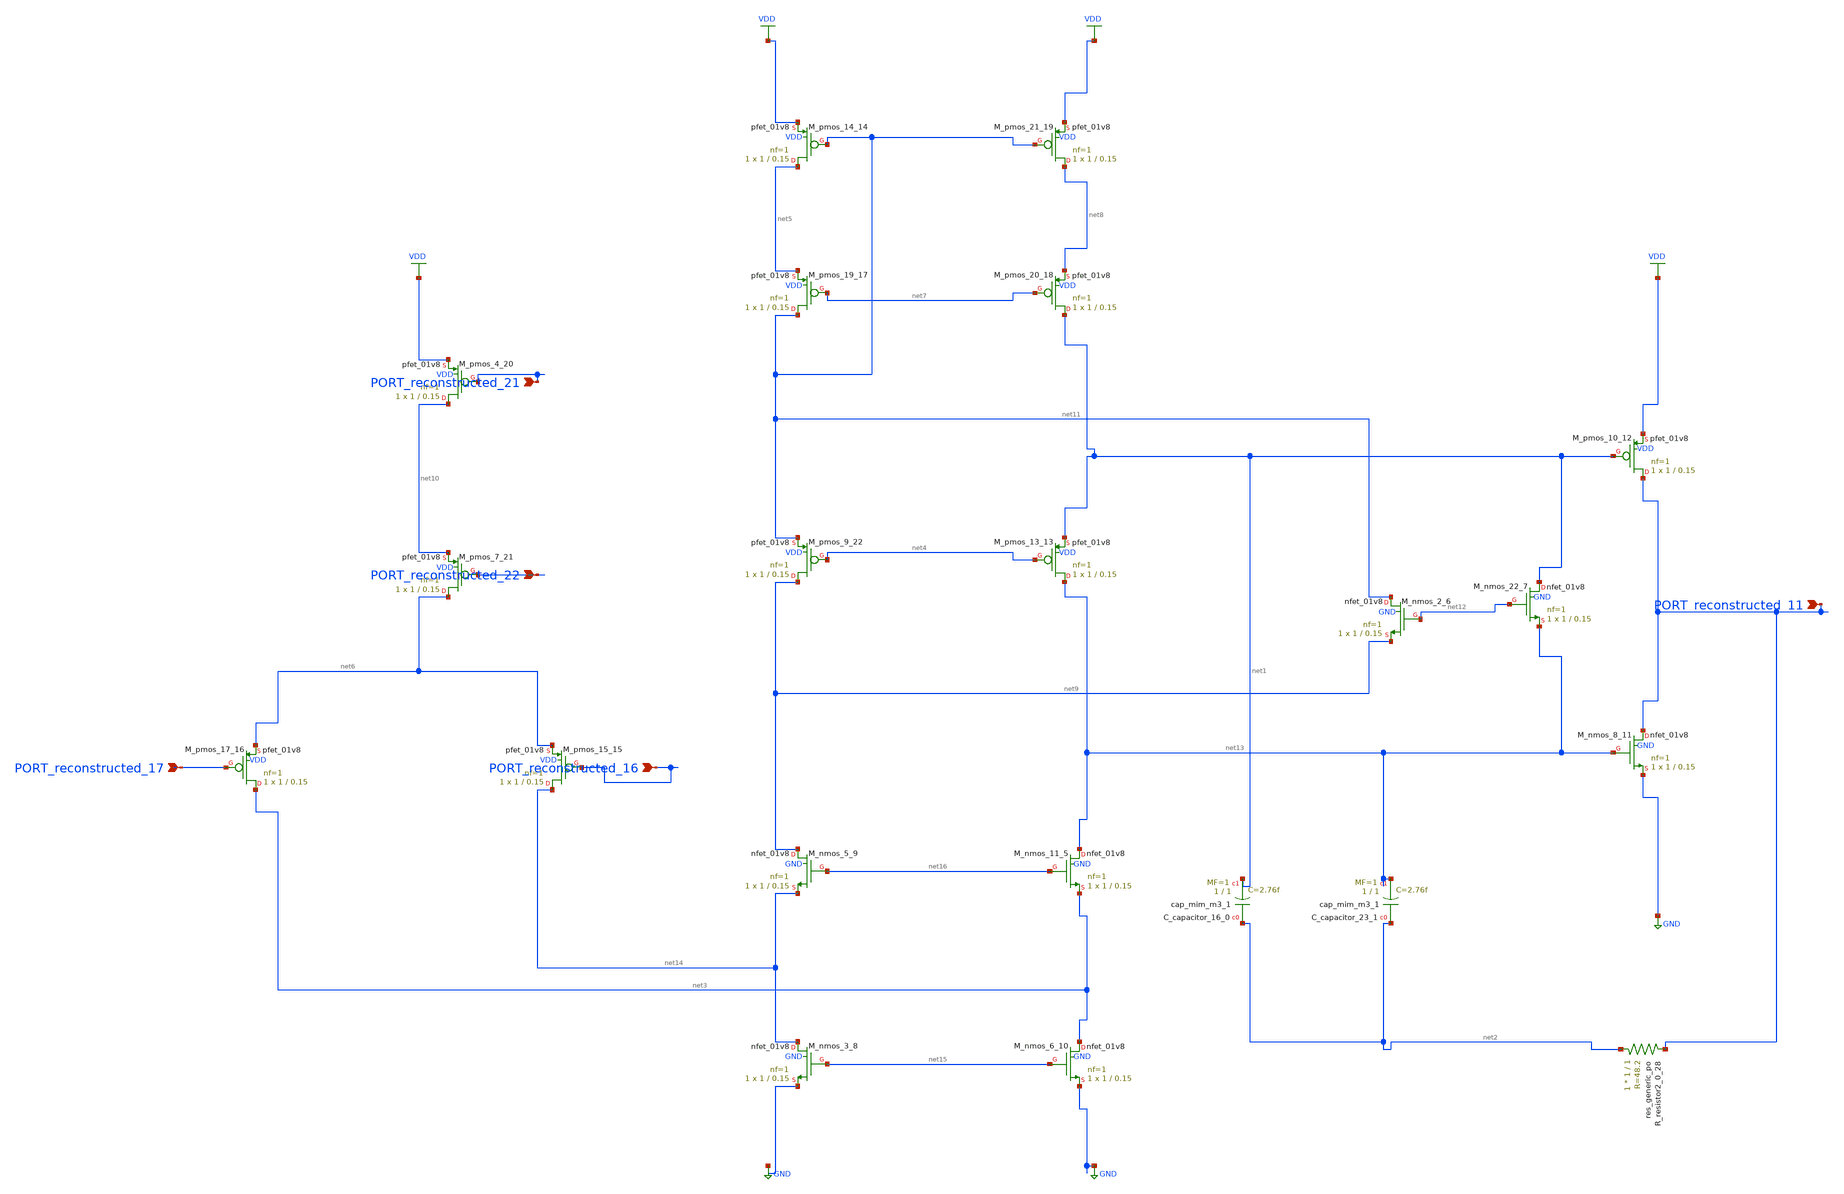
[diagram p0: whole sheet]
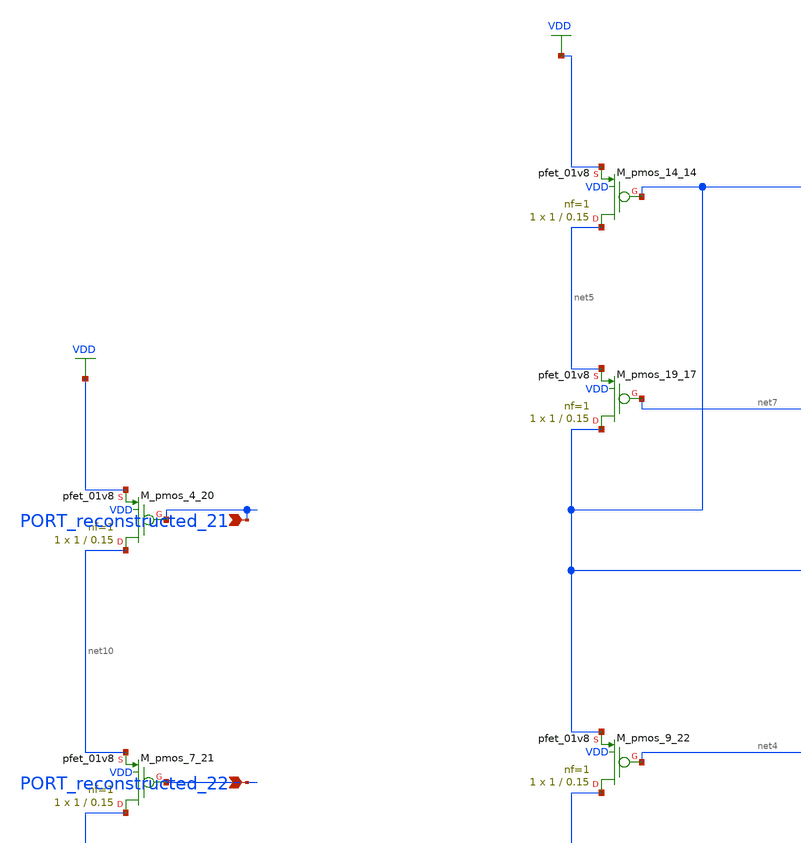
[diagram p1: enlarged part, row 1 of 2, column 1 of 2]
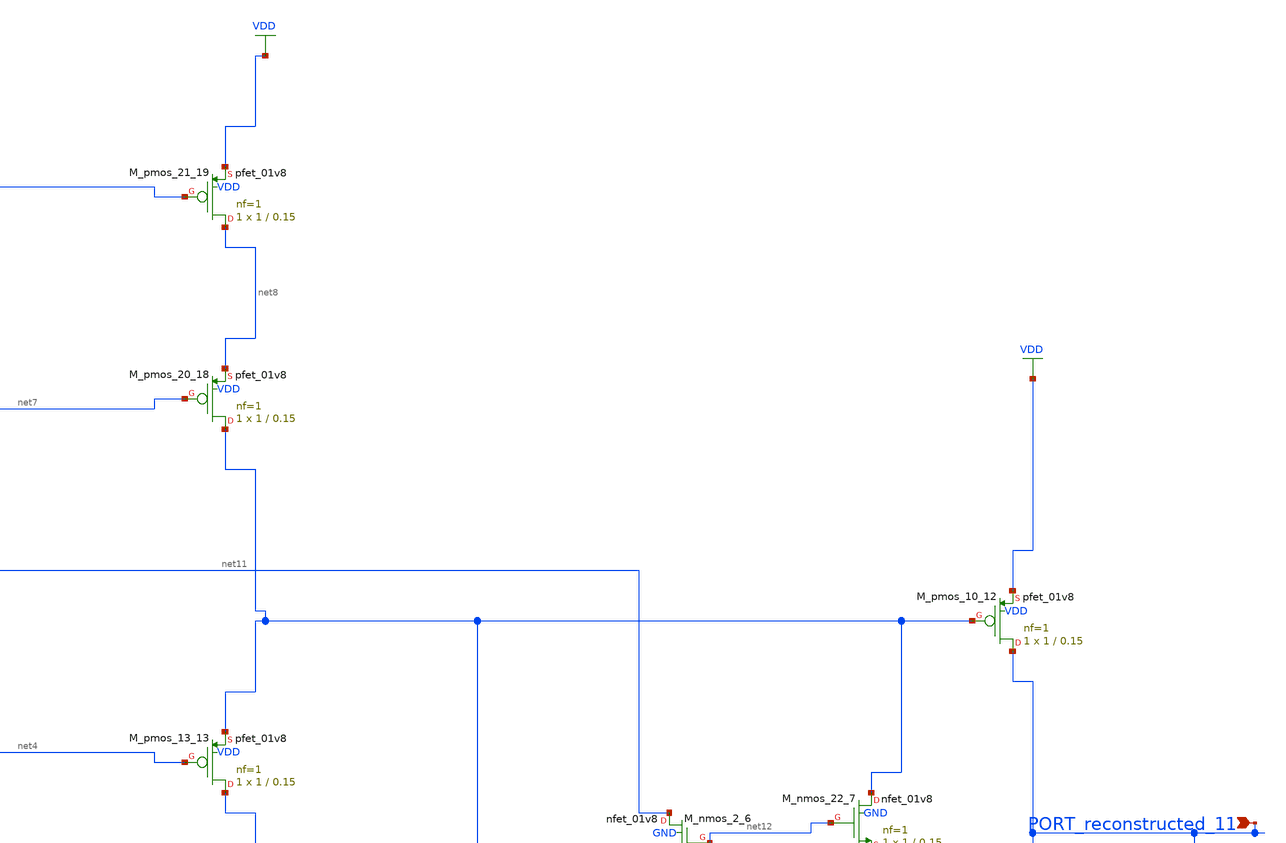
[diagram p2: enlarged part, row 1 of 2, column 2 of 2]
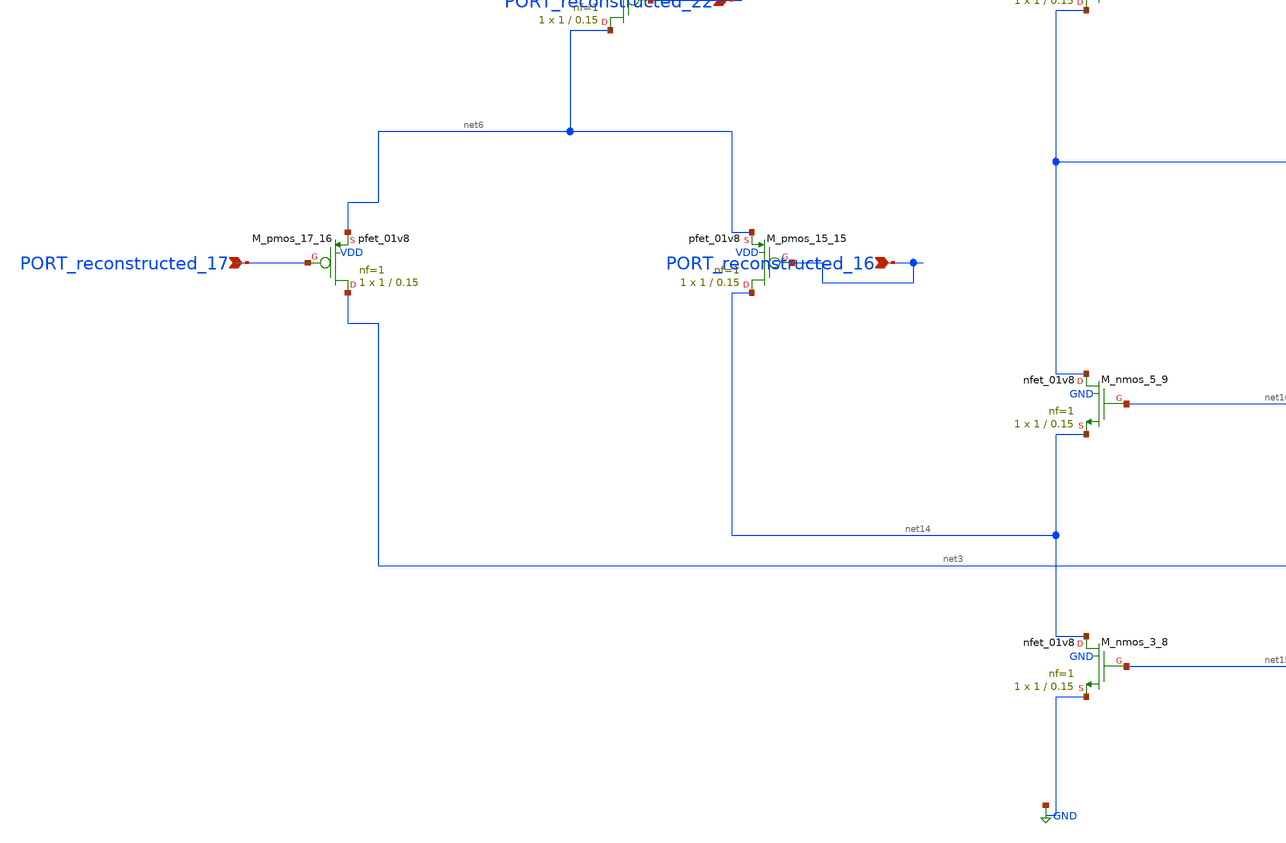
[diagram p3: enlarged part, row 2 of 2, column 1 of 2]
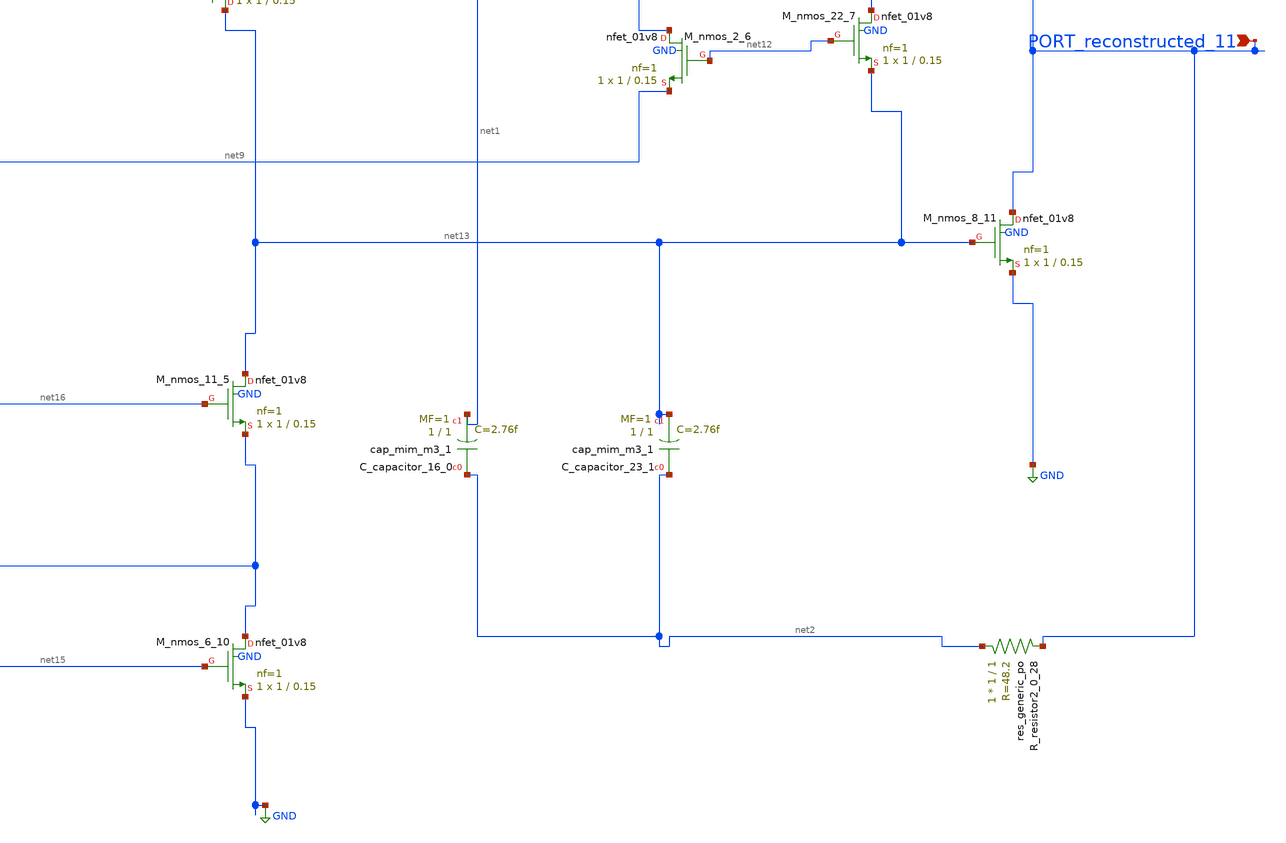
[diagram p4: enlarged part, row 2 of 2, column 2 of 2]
** sch_path: schematics/SchemGen/p07_fig3_filter_opamp.sch
**.subckt p07_fig3_filter_opamp PORT_reconstructed_17 PORT_reconstructed_11 PORT_reconstructed_22
*+ PORT_reconstructed_16 PORT_reconstructed_21
*.ipin PORT_reconstructed_17
*.ipin PORT_reconstructed_11
*.ipin PORT_reconstructed_22
*.ipin PORT_reconstructed_16
*.ipin PORT_reconstructed_21
XC_capacitor_16_0 net2 net1 sky130_fd_pr__cap_mim_m3_1 W=1 L=1 MF=1 m=1
XC_capacitor_23_1 net2 net13 sky130_fd_pr__cap_mim_m3_1 W=1 L=1 MF=1 m=1
XM_nmos_11_5 net13 net16 net3 GND sky130_fd_pr__nfet_01v8 L=0.15 W=1 nf=1 ad='int((1 + 1)/2) * 1 / 1 * 0.29'
+ as='int((1 + 2)/2) * 1 / 1 * 0.29' pd='2*int((1 + 1)/2) * (1 / 1 + 0.29)' ps='2*int((1 + 2)/2) * (1 / 1 + 0.29)'
+ nrd='0.29 / 1 ' nrs='0.29 / 1 ' sa=0 sb=0 sd=0 mult=1 m=1
XM_nmos_2_6 net11 net12 net9 GND sky130_fd_pr__nfet_01v8 L=0.15 W=1 nf=1 ad='int((1 + 1)/2) * 1 / 1 * 0.29'
+ as='int((1 + 2)/2) * 1 / 1 * 0.29' pd='2*int((1 + 1)/2) * (1 / 1 + 0.29)' ps='2*int((1 + 2)/2) * (1 / 1 + 0.29)'
+ nrd='0.29 / 1 ' nrs='0.29 / 1 ' sa=0 sb=0 sd=0 mult=1 m=1
XM_nmos_22_7 net1 net12 net13 GND sky130_fd_pr__nfet_01v8 L=0.15 W=1 nf=1 ad='int((1 + 1)/2) * 1 / 1 * 0.29'
+ as='int((1 + 2)/2) * 1 / 1 * 0.29' pd='2*int((1 + 1)/2) * (1 / 1 + 0.29)' ps='2*int((1 + 2)/2) * (1 / 1 + 0.29)'
+ nrd='0.29 / 1 ' nrs='0.29 / 1 ' sa=0 sb=0 sd=0 mult=1 m=1
XM_nmos_3_8 net14 net15 GND GND sky130_fd_pr__nfet_01v8 L=0.15 W=1 nf=1 ad='int((1 + 1)/2) * 1 / 1 * 0.29'
+ as='int((1 + 2)/2) * 1 / 1 * 0.29' pd='2*int((1 + 1)/2) * (1 / 1 + 0.29)' ps='2*int((1 + 2)/2) * (1 / 1 + 0.29)'
+ nrd='0.29 / 1 ' nrs='0.29 / 1 ' sa=0 sb=0 sd=0 mult=1 m=1
XM_nmos_5_9 net9 net16 net14 GND sky130_fd_pr__nfet_01v8 L=0.15 W=1 nf=1 ad='int((1 + 1)/2) * 1 / 1 * 0.29'
+ as='int((1 + 2)/2) * 1 / 1 * 0.29' pd='2*int((1 + 1)/2) * (1 / 1 + 0.29)' ps='2*int((1 + 2)/2) * (1 / 1 + 0.29)'
+ nrd='0.29 / 1 ' nrs='0.29 / 1 ' sa=0 sb=0 sd=0 mult=1 m=1
XM_nmos_6_10 net3 net15 GND GND sky130_fd_pr__nfet_01v8 L=0.15 W=1 nf=1 ad='int((1 + 1)/2) * 1 / 1 * 0.29'
+ as='int((1 + 2)/2) * 1 / 1 * 0.29' pd='2*int((1 + 1)/2) * (1 / 1 + 0.29)' ps='2*int((1 + 2)/2) * (1 / 1 + 0.29)'
+ nrd='0.29 / 1 ' nrs='0.29 / 1 ' sa=0 sb=0 sd=0 mult=1 m=1
XM_nmos_8_11 PORT_reconstructed_11 net13 GND GND sky130_fd_pr__nfet_01v8 L=0.15 W=1 nf=1 ad='int((1 + 1)/2) * 1 / 1 * 0.29'
+ as='int((1 + 2)/2) * 1 / 1 * 0.29' pd='2*int((1 + 1)/2) * (1 / 1 + 0.29)' ps='2*int((1 + 2)/2) * (1 / 1 + 0.29)'
+ nrd='0.29 / 1 ' nrs='0.29 / 1 ' sa=0 sb=0 sd=0 mult=1 m=1
XM_pmos_10_12 PORT_reconstructed_11 net1 VDD VDD sky130_fd_pr__pfet_01v8 L=0.15 W=1 nf=1 ad='int((1 + 1)/2) * 1 / 1 * 0.29'
+ as='int((1 + 2)/2) * 1 / 1 * 0.29' pd='2*int((1 + 1)/2) * (1 / 1 + 0.29)' ps='2*int((1 + 2)/2) * (1 / 1 + 0.29)'
+ nrd='0.29 / 1 ' nrs='0.29 / 1 ' sa=0 sb=0 sd=0 mult=1 m=1
XM_pmos_13_13 net13 net4 net1 VDD sky130_fd_pr__pfet_01v8 L=0.15 W=1 nf=1 ad='int((1 + 1)/2) * 1 / 1 * 0.29'
+ as='int((1 + 2)/2) * 1 / 1 * 0.29' pd='2*int((1 + 1)/2) * (1 / 1 + 0.29)' ps='2*int((1 + 2)/2) * (1 / 1 + 0.29)'
+ nrd='0.29 / 1 ' nrs='0.29 / 1 ' sa=0 sb=0 sd=0 mult=1 m=1
XM_pmos_14_14 net5 net11 VDD VDD sky130_fd_pr__pfet_01v8 L=0.15 W=1 nf=1 ad='int((1 + 1)/2) * 1 / 1 * 0.29'
+ as='int((1 + 2)/2) * 1 / 1 * 0.29' pd='2*int((1 + 1)/2) * (1 / 1 + 0.29)' ps='2*int((1 + 2)/2) * (1 / 1 + 0.29)'
+ nrd='0.29 / 1 ' nrs='0.29 / 1 ' sa=0 sb=0 sd=0 mult=1 m=1
XM_pmos_15_15 net14 PORT_reconstructed_16 net6 VDD sky130_fd_pr__pfet_01v8 L=0.15 W=1 nf=1 ad='int((1 + 1)/2) * 1 / 1 * 0.29'
+ as='int((1 + 2)/2) * 1 / 1 * 0.29' pd='2*int((1 + 1)/2) * (1 / 1 + 0.29)' ps='2*int((1 + 2)/2) * (1 / 1 + 0.29)'
+ nrd='0.29 / 1 ' nrs='0.29 / 1 ' sa=0 sb=0 sd=0 mult=1 m=1
XM_pmos_17_16 net3 PORT_reconstructed_17 net6 VDD sky130_fd_pr__pfet_01v8 L=0.15 W=1 nf=1 ad='int((1 + 1)/2) * 1 / 1 * 0.29'
+ as='int((1 + 2)/2) * 1 / 1 * 0.29' pd='2*int((1 + 1)/2) * (1 / 1 + 0.29)' ps='2*int((1 + 2)/2) * (1 / 1 + 0.29)'
+ nrd='0.29 / 1 ' nrs='0.29 / 1 ' sa=0 sb=0 sd=0 mult=1 m=1
XM_pmos_19_17 net11 net7 net5 VDD sky130_fd_pr__pfet_01v8 L=0.15 W=1 nf=1 ad='int((1 + 1)/2) * 1 / 1 * 0.29'
+ as='int((1 + 2)/2) * 1 / 1 * 0.29' pd='2*int((1 + 1)/2) * (1 / 1 + 0.29)' ps='2*int((1 + 2)/2) * (1 / 1 + 0.29)'
+ nrd='0.29 / 1 ' nrs='0.29 / 1 ' sa=0 sb=0 sd=0 mult=1 m=1
XM_pmos_20_18 net1 net7 net8 VDD sky130_fd_pr__pfet_01v8 L=0.15 W=1 nf=1 ad='int((1 + 1)/2) * 1 / 1 * 0.29'
+ as='int((1 + 2)/2) * 1 / 1 * 0.29' pd='2*int((1 + 1)/2) * (1 / 1 + 0.29)' ps='2*int((1 + 2)/2) * (1 / 1 + 0.29)'
+ nrd='0.29 / 1 ' nrs='0.29 / 1 ' sa=0 sb=0 sd=0 mult=1 m=1
XM_pmos_21_19 net8 net11 VDD VDD sky130_fd_pr__pfet_01v8 L=0.15 W=1 nf=1 ad='int((1 + 1)/2) * 1 / 1 * 0.29'
+ as='int((1 + 2)/2) * 1 / 1 * 0.29' pd='2*int((1 + 1)/2) * (1 / 1 + 0.29)' ps='2*int((1 + 2)/2) * (1 / 1 + 0.29)'
+ nrd='0.29 / 1 ' nrs='0.29 / 1 ' sa=0 sb=0 sd=0 mult=1 m=1
XM_pmos_4_20 net10 PORT_reconstructed_21 VDD VDD sky130_fd_pr__pfet_01v8 L=0.15 W=1 nf=1 ad='int((1 + 1)/2) * 1 / 1 * 0.29'
+ as='int((1 + 2)/2) * 1 / 1 * 0.29' pd='2*int((1 + 1)/2) * (1 / 1 + 0.29)' ps='2*int((1 + 2)/2) * (1 / 1 + 0.29)'
+ nrd='0.29 / 1 ' nrs='0.29 / 1 ' sa=0 sb=0 sd=0 mult=1 m=1
XM_pmos_7_21 net6 PORT_reconstructed_22 net10 VDD sky130_fd_pr__pfet_01v8 L=0.15 W=1 nf=1 ad='int((1 + 1)/2) * 1 / 1 * 0.29'
+ as='int((1 + 2)/2) * 1 / 1 * 0.29' pd='2*int((1 + 1)/2) * (1 / 1 + 0.29)' ps='2*int((1 + 2)/2) * (1 / 1 + 0.29)'
+ nrd='0.29 / 1 ' nrs='0.29 / 1 ' sa=0 sb=0 sd=0 mult=1 m=1
XM_pmos_9_22 net9 net4 net11 VDD sky130_fd_pr__pfet_01v8 L=0.15 W=1 nf=1 ad='int((1 + 1)/2) * 1 / 1 * 0.29'
+ as='int((1 + 2)/2) * 1 / 1 * 0.29' pd='2*int((1 + 1)/2) * (1 / 1 + 0.29)' ps='2*int((1 + 2)/2) * (1 / 1 + 0.29)'
+ nrd='0.29 / 1 ' nrs='0.29 / 1 ' sa=0 sb=0 sd=0 mult=1 m=1
XR_resistor2_0_28 net2 PORT_reconstructed_11 sky130_fd_pr__res_generic_po W=1 L=1 m=1
**.ends
.GLOBAL GND
.GLOBAL VDD
.end
